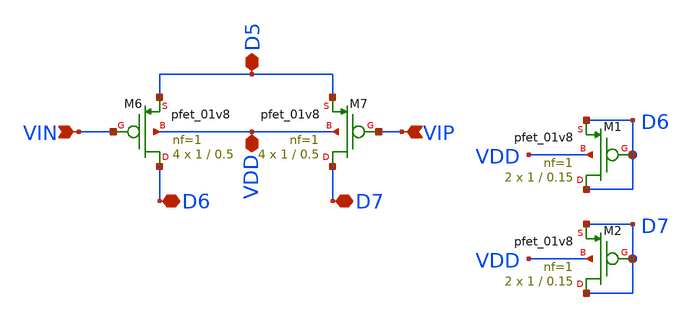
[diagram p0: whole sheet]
** sch_path: opamp1stage/magic/difpair.sch
**.subckt difpair VIN VIP D6 D7 D5 VDD
*.ipin VIN
*.ipin VIP
*.iopin D6
*.iopin D7
*.iopin D5
*.iopin VDD
XM6 D6 VIN D5 VDD sky130_fd_pr__pfet_01v8 L=0.5 W=1 nf=1 ad='int((nf+1)/2) * W/nf * 0.29' as='int((nf+2)/2) * W/nf * 0.29'
+ pd='2*int((nf+1)/2) * (W/nf + 0.29)' ps='2*int((nf+2)/2) * (W/nf + 0.29)' nrd='0.29 / W' nrs='0.29 / W'
+ sa=0 sb=0 sd=0 mult=4 m=4
XM7 D7 VIP D5 VDD sky130_fd_pr__pfet_01v8 L=0.5 W=1 nf=1 ad='int((nf+1)/2) * W/nf * 0.29' as='int((nf+2)/2) * W/nf * 0.29'
+ pd='2*int((nf+1)/2) * (W/nf + 0.29)' ps='2*int((nf+2)/2) * (W/nf + 0.29)' nrd='0.29 / W' nrs='0.29 / W'
+ sa=0 sb=0 sd=0 mult=4 m=4
XM1 D6 D6 D6 VDD sky130_fd_pr__pfet_01v8 L=0.15 W=1 nf=1 ad='int((nf+1)/2) * W/nf * 0.29' as='int((nf+2)/2) * W/nf * 0.29'
+ pd='2*int((nf+1)/2) * (W/nf + 0.29)' ps='2*int((nf+2)/2) * (W/nf + 0.29)' nrd='0.29 / W' nrs='0.29 / W'
+ sa=0 sb=0 sd=0 mult=2 m=2
XM2 D7 D7 D7 VDD sky130_fd_pr__pfet_01v8 L=0.15 W=1 nf=1 ad='int((nf+1)/2) * W/nf * 0.29' as='int((nf+2)/2) * W/nf * 0.29'
+ pd='2*int((nf+1)/2) * (W/nf + 0.29)' ps='2*int((nf+2)/2) * (W/nf + 0.29)' nrd='0.29 / W' nrs='0.29 / W'
+ sa=0 sb=0 sd=0 mult=2 m=2
**.ends
.end
